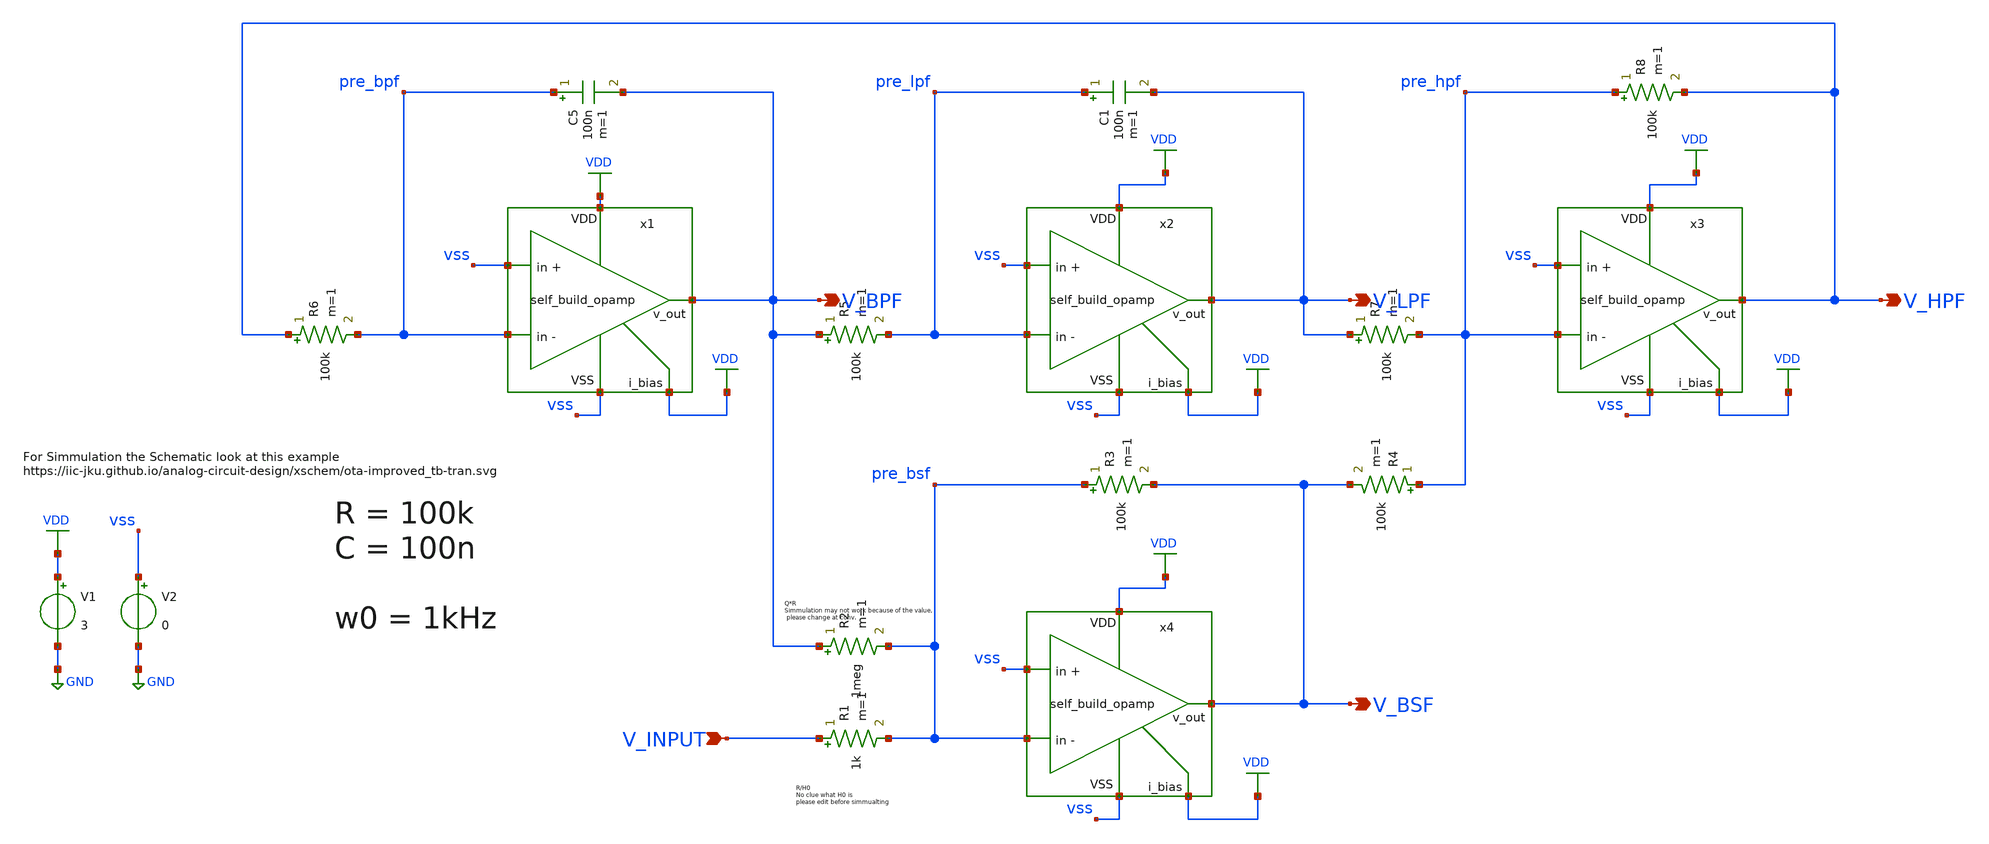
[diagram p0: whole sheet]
** sch_path: 3_Real_Cir/top_level.sch
**.subckt top_level V_BPF V_LPF V_HPF V_BSF V_INPUT
*.opin V_BPF
*.opin V_LPF
*.opin V_HPF
*.opin V_BSF
*.ipin V_INPUT
R1 V_INPUT pre_bsf 1k m=1
R2 V_BPF pre_bsf 1meg m=1
R3 pre_bsf V_BSF 100k m=1
R4 pre_hpf V_BSF 100k m=1
R5 V_BPF pre_lpf 100k m=1
R6 V_HPF pre_bpf 100k m=1
C5 pre_bpf V_BPF 100n m=1
R7 V_LPF pre_hpf 100k m=1
R8 pre_hpf V_HPF 100k m=1
C1 pre_lpf V_LPF 100n m=1
V1 VDD GND 3
V2 vss GND 0
x1 V_BPF vss pre_bpf VDD VDD vss self_build_opamp
x2 V_LPF vss pre_lpf VDD VDD vss self_build_opamp
x3 V_HPF vss pre_hpf VDD VDD vss self_build_opamp
x4 V_BSF vss pre_bsf VDD VDD vss self_build_opamp
**.ends

* expanding   symbol:  self_build_opamp.sym # of pins=6
** sym_path: 3_Real_Cir/self_build_opamp.sym
** sch_path: 3_Real_Cir/self_build_opamp.sch
.subckt self_build_opamp v_out in+ in- i_bias VDD VSS
*.ipin in+
*.ipin in-
*.opin v_out
*.iopin VDD
*.iopin VSS
*.ipin i_bias
XM3 v_imirror in+ v_amp v_amp sg13_hv_nmos w=0.3u l=0.45u ng=1 m=1 mm_ok=1
XM2 v_out in- v_amp v_amp sg13_hv_nmos w=0.3u l=0.45u ng=1 m=1 mm_ok=1
XM4 v_amp i_bias VSS VSS sg13_hv_nmos w=0.3u l=0.45u ng=1 m=1 mm_ok=1
XM5 v_imirror v_imirror VDD VDD sg13_hv_pmos w=0.3u l=0.4u ng=1 m=1 mm_ok=1
XM1 v_out v_imirror VDD VDD sg13_hv_pmos w=0.3u l=0.4u ng=1 m=1 mm_ok=1
XM6 i_bias i_bias VSS VSS sg13_hv_nmos w=0.3u l=0.45u ng=1 m=1 mm_ok=1
.ends

.GLOBAL VDD
.GLOBAL GND
.end
